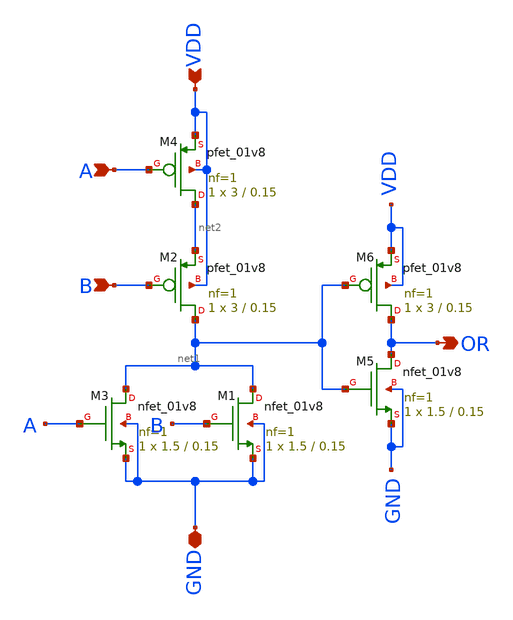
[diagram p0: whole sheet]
** sch_path: skywater_stuff/untitled-5.sch
**.subckt untitled-5 A B OR GND VDD
*.ipin A
*.ipin B
*.opin OR
*.iopin GND
*.ipin VDD
XM3 net1 A GND GND sky130_fd_pr__nfet_01v8 L=0.15 W=1.5 nf=1 ad='int((nf+1)/2) * W/nf * 0.29' as='int((nf+2)/2) * W/nf * 0.29'
+ pd='2*int((nf+1)/2) * (W/nf + 0.29)' ps='2*int((nf+2)/2) * (W/nf + 0.29)' nrd='0.29 / W' nrs='0.29 / W'
+ sa=0 sb=0 sd=0 mult=1 m=1
XM4 net2 A VDD VDD sky130_fd_pr__pfet_01v8 L=0.15 W=3 nf=1 ad='int((nf+1)/2) * W/nf * 0.29' as='int((nf+2)/2) * W/nf * 0.29'
+ pd='2*int((nf+1)/2) * (W/nf + 0.29)' ps='2*int((nf+2)/2) * (W/nf + 0.29)' nrd='0.29 / W' nrs='0.29 / W'
+ sa=0 sb=0 sd=0 mult=1 m=1
XM2 net1 B net2 VDD sky130_fd_pr__pfet_01v8 L=0.15 W=3 nf=1 ad='int((nf+1)/2) * W/nf * 0.29' as='int((nf+2)/2) * W/nf * 0.29'
+ pd='2*int((nf+1)/2) * (W/nf + 0.29)' ps='2*int((nf+2)/2) * (W/nf + 0.29)' nrd='0.29 / W' nrs='0.29 / W'
+ sa=0 sb=0 sd=0 mult=1 m=1
XM5 OR net1 GND GND sky130_fd_pr__nfet_01v8 L=0.15 W=1.5 nf=1 ad='int((nf+1)/2) * W/nf * 0.29' as='int((nf+2)/2) * W/nf * 0.29'
+ pd='2*int((nf+1)/2) * (W/nf + 0.29)' ps='2*int((nf+2)/2) * (W/nf + 0.29)' nrd='0.29 / W' nrs='0.29 / W'
+ sa=0 sb=0 sd=0 mult=1 m=1
XM1 net1 B GND GND sky130_fd_pr__nfet_01v8 L=0.15 W=1.5 nf=1 ad='int((nf+1)/2) * W/nf * 0.29' as='int((nf+2)/2) * W/nf * 0.29'
+ pd='2*int((nf+1)/2) * (W/nf + 0.29)' ps='2*int((nf+2)/2) * (W/nf + 0.29)' nrd='0.29 / W' nrs='0.29 / W'
+ sa=0 sb=0 sd=0 mult=1 m=1
XM6 OR net1 VDD VDD sky130_fd_pr__pfet_01v8 L=0.15 W=3 nf=1 ad='int((nf+1)/2) * W/nf * 0.29' as='int((nf+2)/2) * W/nf * 0.29'
+ pd='2*int((nf+1)/2) * (W/nf + 0.29)' ps='2*int((nf+2)/2) * (W/nf + 0.29)' nrd='0.29 / W' nrs='0.29 / W'
+ sa=0 sb=0 sd=0 mult=1 m=1
**.ends
.end
